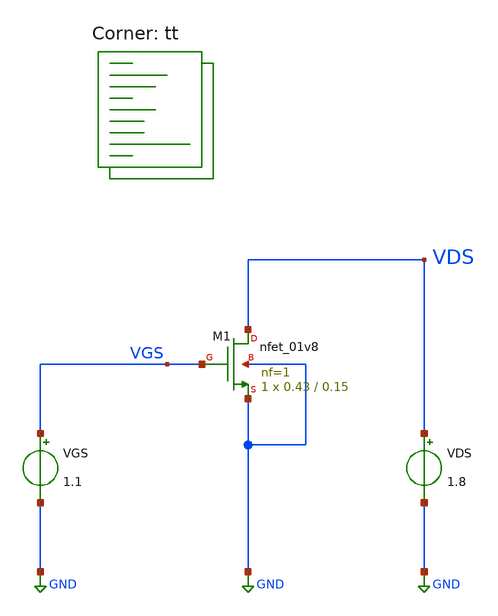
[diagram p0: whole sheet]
** sch_path: projects/bandgapref/xschem_ngspice/new_files/gm_id_check_2.sch
**.subckt gm_id_check_2
XM1 VDS VGS GND GND sky130_fd_pr__nfet_01v8 L=0.15 W=0.43 nf=1 ad='int((nf+1)/2) * W/nf * 0.29' as='int((nf+2)/2) * W/nf * 0.29'
+ pd='2*int((nf+1)/2) * (W/nf + 0.29)' ps='2*int((nf+2)/2) * (W/nf + 0.29)' nrd='0.29 / W' nrs='0.29 / W'
+ sa=0 sb=0 sd=0 mult=1 m=1
VGS VGS GND 1.1
VDS VDS GND 1.8
**** begin user architecture code
.lib $::SKYWATER_MODELS/sky130.lib.spice tt



.option method=gear
.option wnflag=1
.option savecurrents

.save @m.xm1.msky130_fd_pr__nfet_01v8[gm]

.control

  let w_value = 1
  let final_w_value = 10
  let increment = 1
  let index = 1

  dowhile w_value <= final_w_value

    alter @m.xm1.msky130_fd_pr__nfet_01v8[w] = w_value
    save @m.xm1.msky130_fd_pr__nfet_01v8[w]
    remzerovec
    *linearize i(vds)
    echo $&w_value
    write gm_id_check_2_{$&index}.raw
    * wrdata /foss/designs/my_design/projects/bandgapref/xschem_ngspice/new_files/gm_id_check_2_{$&index}.txt
+ i(vds)
    set appendwrite
    reset
    let index = index + 1
    let w_value = w_value + increment

  end

.endc



**** end user architecture code
**.ends
.GLOBAL GND
.end
